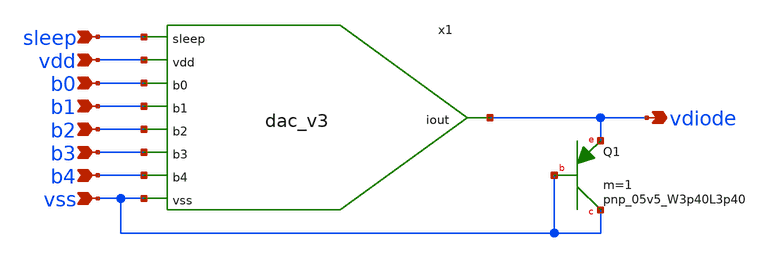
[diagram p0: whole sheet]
** sch_path: design/LELO_TORD_SKY130A/TB_dac_v2.sch
**.subckt TB_dac_v2 b1 b2 b3 b4 b0 vss vdd sleep vdiode
*.ipin b1
*.ipin b2
*.ipin b3
*.ipin b4
*.ipin b0
*.ipin vss
*.ipin vdd
*.ipin sleep
*.opin vdiode
XQ1 vss vss vdiode sky130_fd_pr__pnp_05v5_W3p40L3p40 m=1
x1 sleep vdd b0 b1 b2 b3 b4 vdiode vss dac_v3
**.ends
.end
